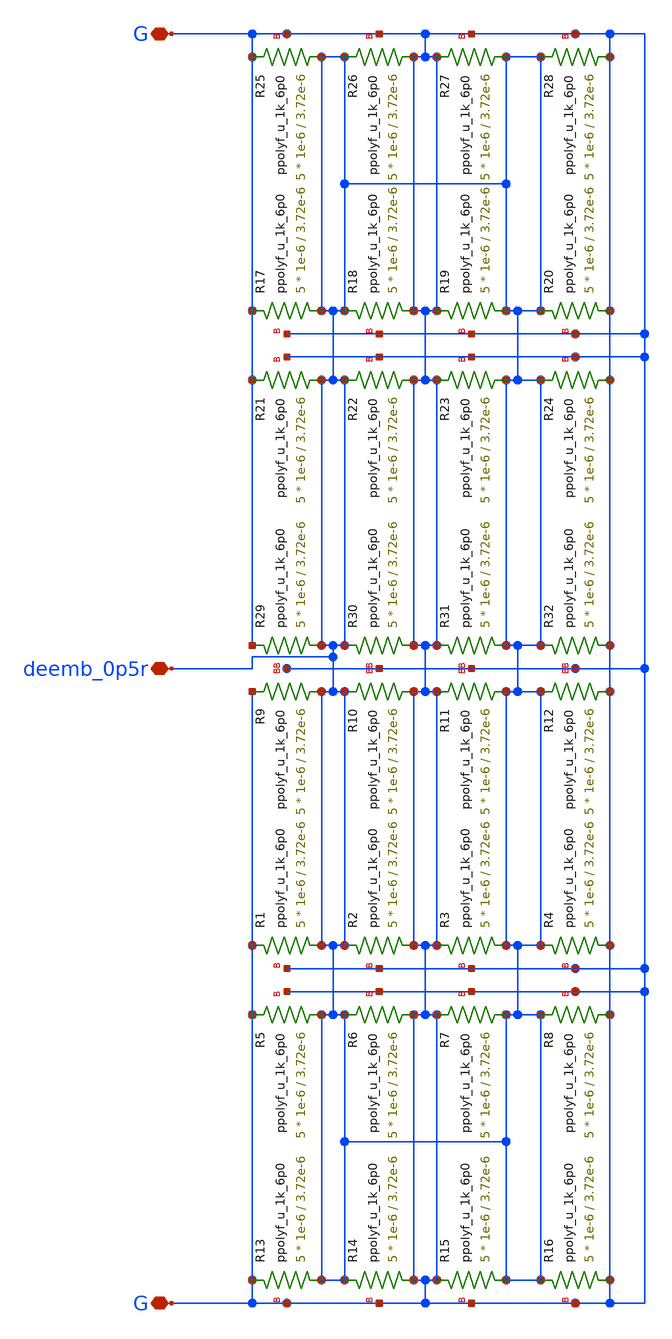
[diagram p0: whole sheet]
** sch_path: xschem/DEEMB_0P5R.sch
**.subckt DEEMB_0P5R G deemb_0p5r G
*.iopin G
*.iopin deemb_0p5r
*.iopin G
XR1 deemb_0p5r G G ppolyf_u_1k_6p0 r_width=1e-6 r_length=3.72e-6 m=5
XR2 G deemb_0p5r G ppolyf_u_1k_6p0 r_width=1e-6 r_length=3.72e-6 m=5
XR3 deemb_0p5r G G ppolyf_u_1k_6p0 r_width=1e-6 r_length=3.72e-6 m=5
XR4 G deemb_0p5r G ppolyf_u_1k_6p0 r_width=1e-6 r_length=3.72e-6 m=5
XR5 deemb_0p5r G G ppolyf_u_1k_6p0 r_width=1e-6 r_length=3.72e-6 m=5
XR6 G deemb_0p5r G ppolyf_u_1k_6p0 r_width=1e-6 r_length=3.72e-6 m=5
XR7 deemb_0p5r G G ppolyf_u_1k_6p0 r_width=1e-6 r_length=3.72e-6 m=5
XR8 G deemb_0p5r G ppolyf_u_1k_6p0 r_width=1e-6 r_length=3.72e-6 m=5
XR9 deemb_0p5r G G ppolyf_u_1k_6p0 r_width=1e-6 r_length=3.72e-6 m=5
XR10 G deemb_0p5r G ppolyf_u_1k_6p0 r_width=1e-6 r_length=3.72e-6 m=5
XR11 deemb_0p5r G G ppolyf_u_1k_6p0 r_width=1e-6 r_length=3.72e-6 m=5
XR12 G deemb_0p5r G ppolyf_u_1k_6p0 r_width=1e-6 r_length=3.72e-6 m=5
XR13 deemb_0p5r G G ppolyf_u_1k_6p0 r_width=1e-6 r_length=3.72e-6 m=5
XR14 G deemb_0p5r G ppolyf_u_1k_6p0 r_width=1e-6 r_length=3.72e-6 m=5
XR15 deemb_0p5r G G ppolyf_u_1k_6p0 r_width=1e-6 r_length=3.72e-6 m=5
XR16 G deemb_0p5r G ppolyf_u_1k_6p0 r_width=1e-6 r_length=3.72e-6 m=5
XR17 deemb_0p5r G G ppolyf_u_1k_6p0 r_width=1e-6 r_length=3.72e-6 m=5
XR18 G deemb_0p5r G ppolyf_u_1k_6p0 r_width=1e-6 r_length=3.72e-6 m=5
XR19 deemb_0p5r G G ppolyf_u_1k_6p0 r_width=1e-6 r_length=3.72e-6 m=5
XR20 G deemb_0p5r G ppolyf_u_1k_6p0 r_width=1e-6 r_length=3.72e-6 m=5
XR21 deemb_0p5r G G ppolyf_u_1k_6p0 r_width=1e-6 r_length=3.72e-6 m=5
XR22 G deemb_0p5r G ppolyf_u_1k_6p0 r_width=1e-6 r_length=3.72e-6 m=5
XR23 deemb_0p5r G G ppolyf_u_1k_6p0 r_width=1e-6 r_length=3.72e-6 m=5
XR24 G deemb_0p5r G ppolyf_u_1k_6p0 r_width=1e-6 r_length=3.72e-6 m=5
XR25 deemb_0p5r G G ppolyf_u_1k_6p0 r_width=1e-6 r_length=3.72e-6 m=5
XR26 G deemb_0p5r G ppolyf_u_1k_6p0 r_width=1e-6 r_length=3.72e-6 m=5
XR27 deemb_0p5r G G ppolyf_u_1k_6p0 r_width=1e-6 r_length=3.72e-6 m=5
XR28 G deemb_0p5r G ppolyf_u_1k_6p0 r_width=1e-6 r_length=3.72e-6 m=5
XR29 deemb_0p5r G G ppolyf_u_1k_6p0 r_width=1e-6 r_length=3.72e-6 m=5
XR30 G deemb_0p5r G ppolyf_u_1k_6p0 r_width=1e-6 r_length=3.72e-6 m=5
XR31 deemb_0p5r G G ppolyf_u_1k_6p0 r_width=1e-6 r_length=3.72e-6 m=5
XR32 G deemb_0p5r G ppolyf_u_1k_6p0 r_width=1e-6 r_length=3.72e-6 m=5
**.ends
.end
